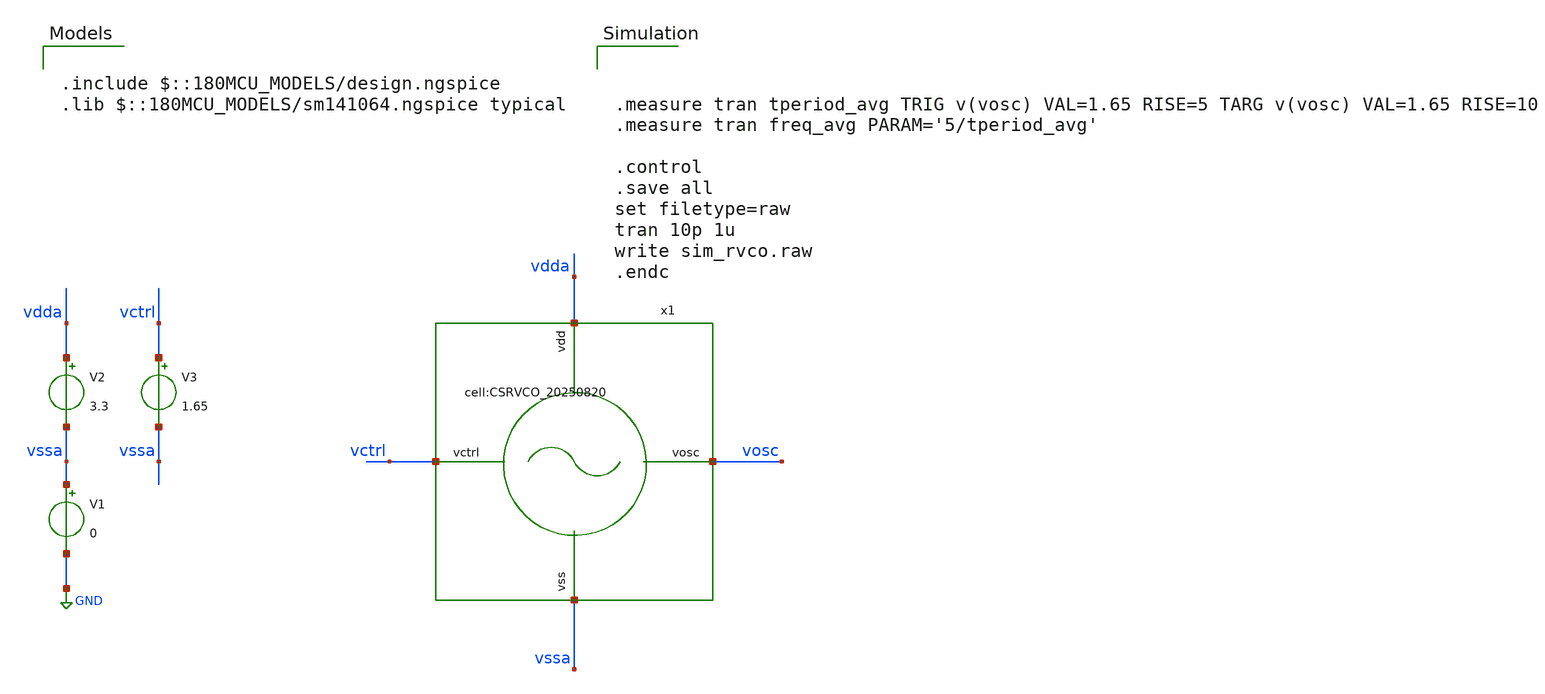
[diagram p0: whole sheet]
** sch_path: designs/libs/tb_analog/tb_CSRVCO/tb_CSRVCO.sch
**.subckt tb_CSRVCO
V1 vssa GND 0
V2 vdda vssa 3.3
V3 vctrl vssa 1.65
x1 vctrl vdda vssa vosc CSRVCO_20250820
**** begin user architecture code

.include $::180MCU_MODELS/design.ngspice
.lib $::180MCU_MODELS/sm141064.ngspice typical




.measure tran tperiod_avg TRIG v(vosc) VAL=1.65 RISE=5 TARG v(vosc) VAL=1.65 RISE=10
.measure tran freq_avg PARAM='5/tperiod_avg'

.control
.save all
set filetype=raw
tran 10p 1u
write sim_rvco.raw
.endc


**** end user architecture code
**.ends
.GLOBAL GND
.end
